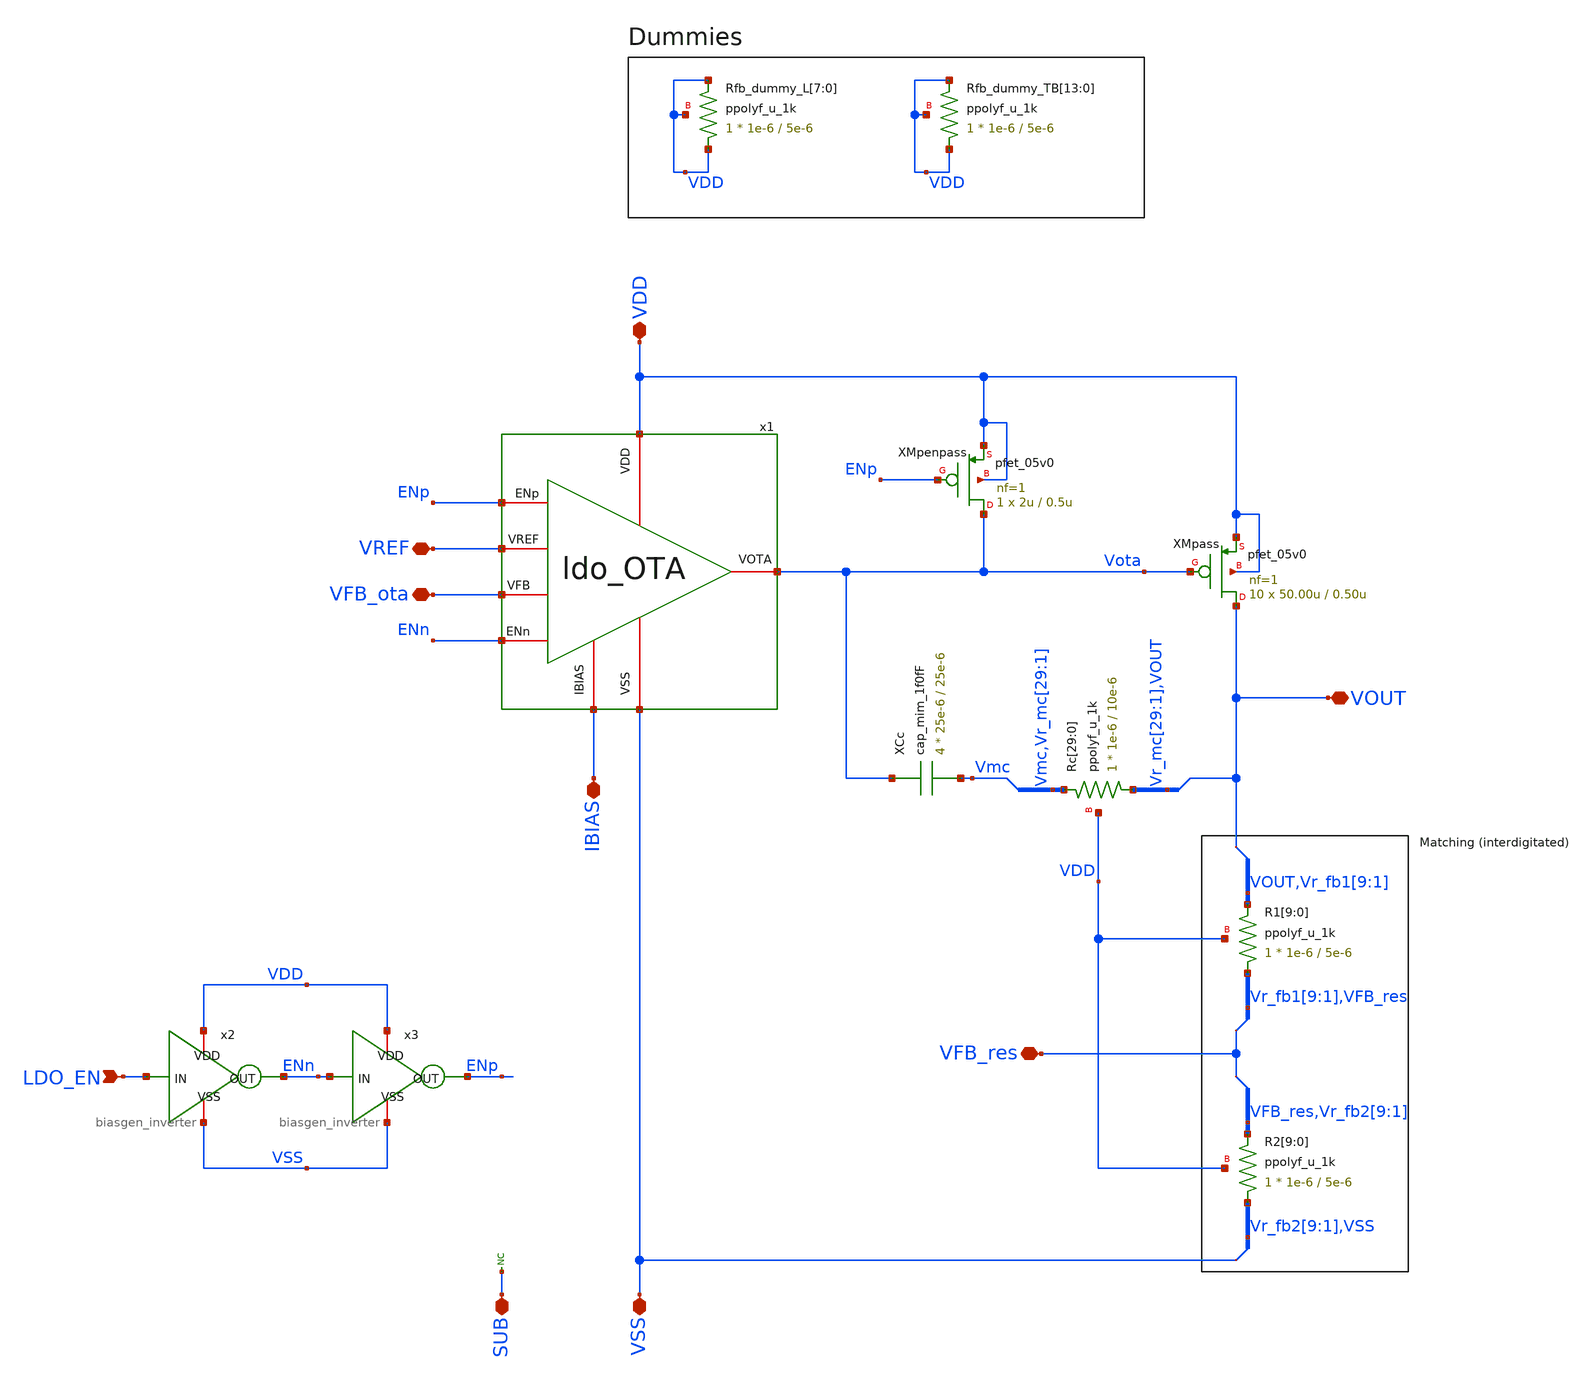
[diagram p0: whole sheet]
** sch_path: designs/libs/core_ldo/ldo/ldo.sch
**.subckt ldo VDD VSS VOUT VREF IBIAS LDO_EN VFB_ota VFB_res SUB
*.iopin VDD
*.iopin VSS
*.iopin VOUT
*.iopin VREF
*.iopin IBIAS
*.ipin LDO_EN
*.iopin VFB_ota
*.iopin VFB_res
*.iopin SUB
XMpass VOUT Vota VDD VDD pfet_05v0 L=0.50u W=50.00u nf=1 ad='int((nf+1)/2) * W/nf * 0.18u' as='int((nf+2)/2) * W/nf * 0.18u'
+ pd='2*int((nf+1)/2) * (W/nf + 0.18u)' ps='2*int((nf+2)/2) * (W/nf + 0.18u)' nrd='0.18u / W' nrs='0.18u / W'
+ sa=0 sb=0 sd=0 m=10
XR1[9] Vr_fb1[9] VOUT VDD ppolyf_u_1k r_width=1e-6 r_length=5e-6 m=1
XR1[8] Vr_fb1[8] Vr_fb1[9] VDD ppolyf_u_1k r_width=1e-6 r_length=5e-6 m=1
XR1[7] Vr_fb1[7] Vr_fb1[8] VDD ppolyf_u_1k r_width=1e-6 r_length=5e-6 m=1
XR1[6] Vr_fb1[6] Vr_fb1[7] VDD ppolyf_u_1k r_width=1e-6 r_length=5e-6 m=1
XR1[5] Vr_fb1[5] Vr_fb1[6] VDD ppolyf_u_1k r_width=1e-6 r_length=5e-6 m=1
XR1[4] Vr_fb1[4] Vr_fb1[5] VDD ppolyf_u_1k r_width=1e-6 r_length=5e-6 m=1
XR1[3] Vr_fb1[3] Vr_fb1[4] VDD ppolyf_u_1k r_width=1e-6 r_length=5e-6 m=1
XR1[2] Vr_fb1[2] Vr_fb1[3] VDD ppolyf_u_1k r_width=1e-6 r_length=5e-6 m=1
XR1[1] Vr_fb1[1] Vr_fb1[2] VDD ppolyf_u_1k r_width=1e-6 r_length=5e-6 m=1
XR1[0] VFB_res Vr_fb1[1] VDD ppolyf_u_1k r_width=1e-6 r_length=5e-6 m=1
XR2[9] Vr_fb2[9] VFB_res VDD ppolyf_u_1k r_width=1e-6 r_length=5e-6 m=1
XR2[8] Vr_fb2[8] Vr_fb2[9] VDD ppolyf_u_1k r_width=1e-6 r_length=5e-6 m=1
XR2[7] Vr_fb2[7] Vr_fb2[8] VDD ppolyf_u_1k r_width=1e-6 r_length=5e-6 m=1
XR2[6] Vr_fb2[6] Vr_fb2[7] VDD ppolyf_u_1k r_width=1e-6 r_length=5e-6 m=1
XR2[5] Vr_fb2[5] Vr_fb2[6] VDD ppolyf_u_1k r_width=1e-6 r_length=5e-6 m=1
XR2[4] Vr_fb2[4] Vr_fb2[5] VDD ppolyf_u_1k r_width=1e-6 r_length=5e-6 m=1
XR2[3] Vr_fb2[3] Vr_fb2[4] VDD ppolyf_u_1k r_width=1e-6 r_length=5e-6 m=1
XR2[2] Vr_fb2[2] Vr_fb2[3] VDD ppolyf_u_1k r_width=1e-6 r_length=5e-6 m=1
XR2[1] Vr_fb2[1] Vr_fb2[2] VDD ppolyf_u_1k r_width=1e-6 r_length=5e-6 m=1
XR2[0] VSS Vr_fb2[1] VDD ppolyf_u_1k r_width=1e-6 r_length=5e-6 m=1
XRc[29] Vr_mc[29] Vmc VDD ppolyf_u_1k r_width=1e-6 r_length=10e-6 m=1
XRc[28] Vr_mc[28] Vr_mc[29] VDD ppolyf_u_1k r_width=1e-6 r_length=10e-6 m=1
XRc[27] Vr_mc[27] Vr_mc[28] VDD ppolyf_u_1k r_width=1e-6 r_length=10e-6 m=1
XRc[26] Vr_mc[26] Vr_mc[27] VDD ppolyf_u_1k r_width=1e-6 r_length=10e-6 m=1
XRc[25] Vr_mc[25] Vr_mc[26] VDD ppolyf_u_1k r_width=1e-6 r_length=10e-6 m=1
XRc[24] Vr_mc[24] Vr_mc[25] VDD ppolyf_u_1k r_width=1e-6 r_length=10e-6 m=1
XRc[23] Vr_mc[23] Vr_mc[24] VDD ppolyf_u_1k r_width=1e-6 r_length=10e-6 m=1
XRc[22] Vr_mc[22] Vr_mc[23] VDD ppolyf_u_1k r_width=1e-6 r_length=10e-6 m=1
XRc[21] Vr_mc[21] Vr_mc[22] VDD ppolyf_u_1k r_width=1e-6 r_length=10e-6 m=1
XRc[20] Vr_mc[20] Vr_mc[21] VDD ppolyf_u_1k r_width=1e-6 r_length=10e-6 m=1
XRc[19] Vr_mc[19] Vr_mc[20] VDD ppolyf_u_1k r_width=1e-6 r_length=10e-6 m=1
XRc[18] Vr_mc[18] Vr_mc[19] VDD ppolyf_u_1k r_width=1e-6 r_length=10e-6 m=1
XRc[17] Vr_mc[17] Vr_mc[18] VDD ppolyf_u_1k r_width=1e-6 r_length=10e-6 m=1
XRc[16] Vr_mc[16] Vr_mc[17] VDD ppolyf_u_1k r_width=1e-6 r_length=10e-6 m=1
XRc[15] Vr_mc[15] Vr_mc[16] VDD ppolyf_u_1k r_width=1e-6 r_length=10e-6 m=1
XRc[14] Vr_mc[14] Vr_mc[15] VDD ppolyf_u_1k r_width=1e-6 r_length=10e-6 m=1
XRc[13] Vr_mc[13] Vr_mc[14] VDD ppolyf_u_1k r_width=1e-6 r_length=10e-6 m=1
XRc[12] Vr_mc[12] Vr_mc[13] VDD ppolyf_u_1k r_width=1e-6 r_length=10e-6 m=1
XRc[11] Vr_mc[11] Vr_mc[12] VDD ppolyf_u_1k r_width=1e-6 r_length=10e-6 m=1
XRc[10] Vr_mc[10] Vr_mc[11] VDD ppolyf_u_1k r_width=1e-6 r_length=10e-6 m=1
XRc[9] Vr_mc[9] Vr_mc[10] VDD ppolyf_u_1k r_width=1e-6 r_length=10e-6 m=1
XRc[8] Vr_mc[8] Vr_mc[9] VDD ppolyf_u_1k r_width=1e-6 r_length=10e-6 m=1
XRc[7] Vr_mc[7] Vr_mc[8] VDD ppolyf_u_1k r_width=1e-6 r_length=10e-6 m=1
XRc[6] Vr_mc[6] Vr_mc[7] VDD ppolyf_u_1k r_width=1e-6 r_length=10e-6 m=1
XRc[5] Vr_mc[5] Vr_mc[6] VDD ppolyf_u_1k r_width=1e-6 r_length=10e-6 m=1
XRc[4] Vr_mc[4] Vr_mc[5] VDD ppolyf_u_1k r_width=1e-6 r_length=10e-6 m=1
XRc[3] Vr_mc[3] Vr_mc[4] VDD ppolyf_u_1k r_width=1e-6 r_length=10e-6 m=1
XRc[2] Vr_mc[2] Vr_mc[3] VDD ppolyf_u_1k r_width=1e-6 r_length=10e-6 m=1
XRc[1] Vr_mc[1] Vr_mc[2] VDD ppolyf_u_1k r_width=1e-6 r_length=10e-6 m=1
XRc[0] VOUT Vr_mc[1] VDD ppolyf_u_1k r_width=1e-6 r_length=10e-6 m=1
XCc Vota Vmc cap_mim_1f0fF c_width=25e-6 c_length=25e-6 m=4
XRfb_dummy_L[7] VDD VDD VDD ppolyf_u_1k r_width=1e-6 r_length=5e-6 m=1
XRfb_dummy_L[6] VDD VDD VDD ppolyf_u_1k r_width=1e-6 r_length=5e-6 m=1
XRfb_dummy_L[5] VDD VDD VDD ppolyf_u_1k r_width=1e-6 r_length=5e-6 m=1
XRfb_dummy_L[4] VDD VDD VDD ppolyf_u_1k r_width=1e-6 r_length=5e-6 m=1
XRfb_dummy_L[3] VDD VDD VDD ppolyf_u_1k r_width=1e-6 r_length=5e-6 m=1
XRfb_dummy_L[2] VDD VDD VDD ppolyf_u_1k r_width=1e-6 r_length=5e-6 m=1
XRfb_dummy_L[1] VDD VDD VDD ppolyf_u_1k r_width=1e-6 r_length=5e-6 m=1
XRfb_dummy_L[0] VDD VDD VDD ppolyf_u_1k r_width=1e-6 r_length=5e-6 m=1
XRfb_dummy_TB[13] VDD VDD VDD ppolyf_u_1k r_width=1e-6 r_length=5e-6 m=1
XRfb_dummy_TB[12] VDD VDD VDD ppolyf_u_1k r_width=1e-6 r_length=5e-6 m=1
XRfb_dummy_TB[11] VDD VDD VDD ppolyf_u_1k r_width=1e-6 r_length=5e-6 m=1
XRfb_dummy_TB[10] VDD VDD VDD ppolyf_u_1k r_width=1e-6 r_length=5e-6 m=1
XRfb_dummy_TB[9] VDD VDD VDD ppolyf_u_1k r_width=1e-6 r_length=5e-6 m=1
XRfb_dummy_TB[8] VDD VDD VDD ppolyf_u_1k r_width=1e-6 r_length=5e-6 m=1
XRfb_dummy_TB[7] VDD VDD VDD ppolyf_u_1k r_width=1e-6 r_length=5e-6 m=1
XRfb_dummy_TB[6] VDD VDD VDD ppolyf_u_1k r_width=1e-6 r_length=5e-6 m=1
XRfb_dummy_TB[5] VDD VDD VDD ppolyf_u_1k r_width=1e-6 r_length=5e-6 m=1
XRfb_dummy_TB[4] VDD VDD VDD ppolyf_u_1k r_width=1e-6 r_length=5e-6 m=1
XRfb_dummy_TB[3] VDD VDD VDD ppolyf_u_1k r_width=1e-6 r_length=5e-6 m=1
XRfb_dummy_TB[2] VDD VDD VDD ppolyf_u_1k r_width=1e-6 r_length=5e-6 m=1
XRfb_dummy_TB[1] VDD VDD VDD ppolyf_u_1k r_width=1e-6 r_length=5e-6 m=1
XRfb_dummy_TB[0] VDD VDD VDD ppolyf_u_1k r_width=1e-6 r_length=5e-6 m=1
* noconn SUB
x2 VDD LDO_EN ENn VSS biasgen_inverter
x3 VDD ENn ENp VSS biasgen_inverter
XMpenpass Vota ENp VDD VDD pfet_05v0 L=0.5u W=2u nf=1 ad='int((nf+1)/2) * W/nf * 0.18u' as='int((nf+2)/2) * W/nf * 0.18u'
+ pd='2*int((nf+1)/2) * (W/nf + 0.18u)' ps='2*int((nf+2)/2) * (W/nf + 0.18u)' nrd='0.18u / W' nrs='0.18u / W'
+ sa=0 sb=0 sd=0 m=1
x1 VDD VREF VFB_ota Vota IBIAS VSS ENp ENn ldo_OTA
**.ends

* expanding   symbol:  libs/core_biasgen/biasgen_inverter/biasgen_inverter.sym # of pins=4
** sym_path: designs/libs/core_biasgen/biasgen_inverter/biasgen_inverter.sym
** sch_path: designs/libs/core_biasgen/biasgen_inverter/biasgen_inverter.sch
.subckt biasgen_inverter VDD IN OUT VSS
*.iopin VDD
*.iopin VSS
*.ipin IN
*.opin OUT
XMINV1 OUT IN VSS VSS nfet_05v0 L=0.60u W=0.50u nf=1 ad='int((nf+1)/2) * W/nf * 0.18u' as='int((nf+2)/2) * W/nf * 0.18u'
+ pd='2*int((nf+1)/2) * (W/nf + 0.18u)' ps='2*int((nf+2)/2) * (W/nf + 0.18u)' nrd='0.18u / W' nrs='0.18u / W'
+ sa=0 sb=0 sd=0 m=1
XMINV2 OUT IN VDD VDD pfet_05v0 L=0.50u W=0.60u nf=1 ad='int((nf+1)/2) * W/nf * 0.18u' as='int((nf+2)/2) * W/nf * 0.18u'
+ pd='2*int((nf+1)/2) * (W/nf + 0.18u)' ps='2*int((nf+2)/2) * (W/nf + 0.18u)' nrd='0.18u / W' nrs='0.18u / W'
+ sa=0 sb=0 sd=0 m=1
.ends


* expanding   symbol:  libs/core_ldo/ldo_OTA/ldo_OTA.sym # of pins=8
** sym_path: designs/libs/core_ldo/ldo_OTA/ldo_OTA.sym
** sch_path: designs/libs/core_ldo/ldo_OTA/ldo_OTA.sch
.subckt ldo_OTA VDD VREF VFB VOTA IBIAS VSS ENp ENn
*.iopin VDD
*.iopin VSS
*.iopin VOTA
*.iopin VREF
*.iopin IBIAS
*.iopin VFB
*.ipin ENp
*.ipin ENn
XM3 Vbp1 Vbp1 VDD VDD pfet_05v0 L=1.00u W=5.50u nf=1 ad='int((nf+1)/2) * W/nf * 0.18u' as='int((nf+2)/2) * W/nf * 0.18u'
+ pd='2*int((nf+1)/2) * (W/nf + 0.18u)' ps='2*int((nf+2)/2) * (W/nf + 0.18u)' nrd='0.18u / W' nrs='0.18u / W'
+ sa=0 sb=0 sd=0 m=2
XM4 Vbp2 Vbp2 VDD VDD pfet_05v0 L=1.00u W=5.50u nf=1 ad='int((nf+1)/2) * W/nf * 0.18u' as='int((nf+2)/2) * W/nf * 0.18u'
+ pd='2*int((nf+1)/2) * (W/nf + 0.18u)' ps='2*int((nf+2)/2) * (W/nf + 0.18u)' nrd='0.18u / W' nrs='0.18u / W'
+ sa=0 sb=0 sd=0 m=2
XM5 Vbn2 Vbp1 VDD VDD pfet_05v0 L=1.00u W=5.50u nf=1 ad='int((nf+1)/2) * W/nf * 0.18u' as='int((nf+2)/2) * W/nf * 0.18u'
+ pd='2*int((nf+1)/2) * (W/nf + 0.18u)' ps='2*int((nf+2)/2) * (W/nf + 0.18u)' nrd='0.18u / W' nrs='0.18u / W'
+ sa=0 sb=0 sd=0 m=2
XM6 VOTA Vbp2 VDD VDD pfet_05v0 L=1.00u W=5.50u nf=1 ad='int((nf+1)/2) * W/nf * 0.18u' as='int((nf+2)/2) * W/nf * 0.18u'
+ pd='2*int((nf+1)/2) * (W/nf + 0.18u)' ps='2*int((nf+2)/2) * (W/nf + 0.18u)' nrd='0.18u / W' nrs='0.18u / W'
+ sa=0 sb=0 sd=0 m=6
XM9 Vbn1 Vbn1 VSS VSS nfet_05v0 L=1.00u W=3.00u nf=1 ad='int((nf+1)/2) * W/nf * 0.18u' as='int((nf+2)/2) * W/nf * 0.18u'
+ pd='2*int((nf+1)/2) * (W/nf + 0.18u)' ps='2*int((nf+2)/2) * (W/nf + 0.18u)' nrd='0.18u / W' nrs='0.18u / W'
+ sa=0 sb=0 sd=0 m=2
XM10 Vtail Vbn1 VSS VSS nfet_05v0 L=1.00u W=3.00u nf=1 ad='int((nf+1)/2) * W/nf * 0.18u' as='int((nf+2)/2) * W/nf * 0.18u'
+ pd='2*int((nf+1)/2) * (W/nf + 0.18u)' ps='2*int((nf+2)/2) * (W/nf + 0.18u)' nrd='0.18u / W' nrs='0.18u / W'
+ sa=0 sb=0 sd=0 m=2
XM7 Vbn2 Vbn2 VSS VSS nfet_05v0 L=1.00u W=1.25u nf=1 ad='int((nf+1)/2) * W/nf * 0.18u' as='int((nf+2)/2) * W/nf * 0.18u'
+ pd='2*int((nf+1)/2) * (W/nf + 0.18u)' ps='2*int((nf+2)/2) * (W/nf + 0.18u)' nrd='0.18u / W' nrs='0.18u / W'
+ sa=0 sb=0 sd=0 m=2
XM8 VOTA Vbn2 VSS VSS nfet_05v0 L=1.00u W=1.25u nf=1 ad='int((nf+1)/2) * W/nf * 0.18u' as='int((nf+2)/2) * W/nf * 0.18u'
+ pd='2*int((nf+1)/2) * (W/nf + 0.18u)' ps='2*int((nf+2)/2) * (W/nf + 0.18u)' nrd='0.18u / W' nrs='0.18u / W'
+ sa=0 sb=0 sd=0 m=6
XM1 Vbp1 VREF Vtail VSS nfet_05v0 L=0.60u W=5.00u nf=1 ad='int((nf+1)/2) * W/nf * 0.18u' as='int((nf+2)/2) * W/nf * 0.18u'
+ pd='2*int((nf+1)/2) * (W/nf + 0.18u)' ps='2*int((nf+2)/2) * (W/nf + 0.18u)' nrd='0.18u / W' nrs='0.18u / W'
+ sa=0 sb=0 sd=0 m=14
XM2 Vbp2 VFB Vtail VSS nfet_05v0 L=0.60u W=5.00u nf=1 ad='int((nf+1)/2) * W/nf * 0.18u' as='int((nf+2)/2) * W/nf * 0.18u'
+ pd='2*int((nf+1)/2) * (W/nf + 0.18u)' ps='2*int((nf+2)/2) * (W/nf + 0.18u)' nrd='0.18u / W' nrs='0.18u / W'
+ sa=0 sb=0 sd=0 m=14
XMpota_dummy_L[3] VDD VDD VDD VDD pfet_05v0 L=1.00u W=5.50u nf=1 ad='int((nf+1)/2) * W/nf * 0.18u' as='int((nf+2)/2) * W/nf * 0.18u'
+ pd='2*int((nf+1)/2) * (W/nf + 0.18u)' ps='2*int((nf+2)/2) * (W/nf + 0.18u)' nrd='0.18u / W' nrs='0.18u / W'
+ sa=0 sb=0 sd=0 m=1
XMpota_dummy_L[2] VDD VDD VDD VDD pfet_05v0 L=1.00u W=5.50u nf=1 ad='int((nf+1)/2) * W/nf * 0.18u' as='int((nf+2)/2) * W/nf * 0.18u'
+ pd='2*int((nf+1)/2) * (W/nf + 0.18u)' ps='2*int((nf+2)/2) * (W/nf + 0.18u)' nrd='0.18u / W' nrs='0.18u / W'
+ sa=0 sb=0 sd=0 m=1
XMpota_dummy_L[1] VDD VDD VDD VDD pfet_05v0 L=1.00u W=5.50u nf=1 ad='int((nf+1)/2) * W/nf * 0.18u' as='int((nf+2)/2) * W/nf * 0.18u'
+ pd='2*int((nf+1)/2) * (W/nf + 0.18u)' ps='2*int((nf+2)/2) * (W/nf + 0.18u)' nrd='0.18u / W' nrs='0.18u / W'
+ sa=0 sb=0 sd=0 m=1
XMpota_dummy_L[0] VDD VDD VDD VDD pfet_05v0 L=1.00u W=5.50u nf=1 ad='int((nf+1)/2) * W/nf * 0.18u' as='int((nf+2)/2) * W/nf * 0.18u'
+ pd='2*int((nf+1)/2) * (W/nf + 0.18u)' ps='2*int((nf+2)/2) * (W/nf + 0.18u)' nrd='0.18u / W' nrs='0.18u / W'
+ sa=0 sb=0 sd=0 m=1
XMpota_dummy_TB[15] VDD VDD VDD VDD pfet_05v0 L=1.00u W=5.50u nf=1 ad='int((nf+1)/2) * W/nf * 0.18u'
+ as='int((nf+2)/2) * W/nf * 0.18u' pd='2*int((nf+1)/2) * (W/nf + 0.18u)' ps='2*int((nf+2)/2) * (W/nf + 0.18u)'
+ nrd='0.18u / W' nrs='0.18u / W' sa=0 sb=0 sd=0 m=1
XMpota_dummy_TB[14] VDD VDD VDD VDD pfet_05v0 L=1.00u W=5.50u nf=1 ad='int((nf+1)/2) * W/nf * 0.18u'
+ as='int((nf+2)/2) * W/nf * 0.18u' pd='2*int((nf+1)/2) * (W/nf + 0.18u)' ps='2*int((nf+2)/2) * (W/nf + 0.18u)'
+ nrd='0.18u / W' nrs='0.18u / W' sa=0 sb=0 sd=0 m=1
XMpota_dummy_TB[13] VDD VDD VDD VDD pfet_05v0 L=1.00u W=5.50u nf=1 ad='int((nf+1)/2) * W/nf * 0.18u'
+ as='int((nf+2)/2) * W/nf * 0.18u' pd='2*int((nf+1)/2) * (W/nf + 0.18u)' ps='2*int((nf+2)/2) * (W/nf + 0.18u)'
+ nrd='0.18u / W' nrs='0.18u / W' sa=0 sb=0 sd=0 m=1
XMpota_dummy_TB[12] VDD VDD VDD VDD pfet_05v0 L=1.00u W=5.50u nf=1 ad='int((nf+1)/2) * W/nf * 0.18u'
+ as='int((nf+2)/2) * W/nf * 0.18u' pd='2*int((nf+1)/2) * (W/nf + 0.18u)' ps='2*int((nf+2)/2) * (W/nf + 0.18u)'
+ nrd='0.18u / W' nrs='0.18u / W' sa=0 sb=0 sd=0 m=1
XMpota_dummy_TB[11] VDD VDD VDD VDD pfet_05v0 L=1.00u W=5.50u nf=1 ad='int((nf+1)/2) * W/nf * 0.18u'
+ as='int((nf+2)/2) * W/nf * 0.18u' pd='2*int((nf+1)/2) * (W/nf + 0.18u)' ps='2*int((nf+2)/2) * (W/nf + 0.18u)'
+ nrd='0.18u / W' nrs='0.18u / W' sa=0 sb=0 sd=0 m=1
XMpota_dummy_TB[10] VDD VDD VDD VDD pfet_05v0 L=1.00u W=5.50u nf=1 ad='int((nf+1)/2) * W/nf * 0.18u'
+ as='int((nf+2)/2) * W/nf * 0.18u' pd='2*int((nf+1)/2) * (W/nf + 0.18u)' ps='2*int((nf+2)/2) * (W/nf + 0.18u)'
+ nrd='0.18u / W' nrs='0.18u / W' sa=0 sb=0 sd=0 m=1
XMpota_dummy_TB[9] VDD VDD VDD VDD pfet_05v0 L=1.00u W=5.50u nf=1 ad='int((nf+1)/2) * W/nf * 0.18u' as='int((nf+2)/2) * W/nf * 0.18u'
+ pd='2*int((nf+1)/2) * (W/nf + 0.18u)' ps='2*int((nf+2)/2) * (W/nf + 0.18u)' nrd='0.18u / W' nrs='0.18u / W'
+ sa=0 sb=0 sd=0 m=1
XMpota_dummy_TB[8] VDD VDD VDD VDD pfet_05v0 L=1.00u W=5.50u nf=1 ad='int((nf+1)/2) * W/nf * 0.18u' as='int((nf+2)/2) * W/nf * 0.18u'
+ pd='2*int((nf+1)/2) * (W/nf + 0.18u)' ps='2*int((nf+2)/2) * (W/nf + 0.18u)' nrd='0.18u / W' nrs='0.18u / W'
+ sa=0 sb=0 sd=0 m=1
XMpota_dummy_TB[7] VDD VDD VDD VDD pfet_05v0 L=1.00u W=5.50u nf=1 ad='int((nf+1)/2) * W/nf * 0.18u' as='int((nf+2)/2) * W/nf * 0.18u'
+ pd='2*int((nf+1)/2) * (W/nf + 0.18u)' ps='2*int((nf+2)/2) * (W/nf + 0.18u)' nrd='0.18u / W' nrs='0.18u / W'
+ sa=0 sb=0 sd=0 m=1
XMpota_dummy_TB[6] VDD VDD VDD VDD pfet_05v0 L=1.00u W=5.50u nf=1 ad='int((nf+1)/2) * W/nf * 0.18u' as='int((nf+2)/2) * W/nf * 0.18u'
+ pd='2*int((nf+1)/2) * (W/nf + 0.18u)' ps='2*int((nf+2)/2) * (W/nf + 0.18u)' nrd='0.18u / W' nrs='0.18u / W'
+ sa=0 sb=0 sd=0 m=1
XMpota_dummy_TB[5] VDD VDD VDD VDD pfet_05v0 L=1.00u W=5.50u nf=1 ad='int((nf+1)/2) * W/nf * 0.18u' as='int((nf+2)/2) * W/nf * 0.18u'
+ pd='2*int((nf+1)/2) * (W/nf + 0.18u)' ps='2*int((nf+2)/2) * (W/nf + 0.18u)' nrd='0.18u / W' nrs='0.18u / W'
+ sa=0 sb=0 sd=0 m=1
XMpota_dummy_TB[4] VDD VDD VDD VDD pfet_05v0 L=1.00u W=5.50u nf=1 ad='int((nf+1)/2) * W/nf * 0.18u' as='int((nf+2)/2) * W/nf * 0.18u'
+ pd='2*int((nf+1)/2) * (W/nf + 0.18u)' ps='2*int((nf+2)/2) * (W/nf + 0.18u)' nrd='0.18u / W' nrs='0.18u / W'
+ sa=0 sb=0 sd=0 m=1
XMpota_dummy_TB[3] VDD VDD VDD VDD pfet_05v0 L=1.00u W=5.50u nf=1 ad='int((nf+1)/2) * W/nf * 0.18u' as='int((nf+2)/2) * W/nf * 0.18u'
+ pd='2*int((nf+1)/2) * (W/nf + 0.18u)' ps='2*int((nf+2)/2) * (W/nf + 0.18u)' nrd='0.18u / W' nrs='0.18u / W'
+ sa=0 sb=0 sd=0 m=1
XMpota_dummy_TB[2] VDD VDD VDD VDD pfet_05v0 L=1.00u W=5.50u nf=1 ad='int((nf+1)/2) * W/nf * 0.18u' as='int((nf+2)/2) * W/nf * 0.18u'
+ pd='2*int((nf+1)/2) * (W/nf + 0.18u)' ps='2*int((nf+2)/2) * (W/nf + 0.18u)' nrd='0.18u / W' nrs='0.18u / W'
+ sa=0 sb=0 sd=0 m=1
XMpota_dummy_TB[1] VDD VDD VDD VDD pfet_05v0 L=1.00u W=5.50u nf=1 ad='int((nf+1)/2) * W/nf * 0.18u' as='int((nf+2)/2) * W/nf * 0.18u'
+ pd='2*int((nf+1)/2) * (W/nf + 0.18u)' ps='2*int((nf+2)/2) * (W/nf + 0.18u)' nrd='0.18u / W' nrs='0.18u / W'
+ sa=0 sb=0 sd=0 m=1
XMpota_dummy_TB[0] VDD VDD VDD VDD pfet_05v0 L=1.00u W=5.50u nf=1 ad='int((nf+1)/2) * W/nf * 0.18u' as='int((nf+2)/2) * W/nf * 0.18u'
+ pd='2*int((nf+1)/2) * (W/nf + 0.18u)' ps='2*int((nf+2)/2) * (W/nf + 0.18u)' nrd='0.18u / W' nrs='0.18u / W'
+ sa=0 sb=0 sd=0 m=1
XMndiff_dummy_L[7] VSS VSS VSS VSS nfet_05v0 L=0.60u W=5.00u nf=1 ad='int((nf+1)/2) * W/nf * 0.18u' as='int((nf+2)/2) * W/nf * 0.18u'
+ pd='2*int((nf+1)/2) * (W/nf + 0.18u)' ps='2*int((nf+2)/2) * (W/nf + 0.18u)' nrd='0.18u / W' nrs='0.18u / W'
+ sa=0 sb=0 sd=0 m=1
XMndiff_dummy_L[6] VSS VSS VSS VSS nfet_05v0 L=0.60u W=5.00u nf=1 ad='int((nf+1)/2) * W/nf * 0.18u' as='int((nf+2)/2) * W/nf * 0.18u'
+ pd='2*int((nf+1)/2) * (W/nf + 0.18u)' ps='2*int((nf+2)/2) * (W/nf + 0.18u)' nrd='0.18u / W' nrs='0.18u / W'
+ sa=0 sb=0 sd=0 m=1
XMndiff_dummy_L[5] VSS VSS VSS VSS nfet_05v0 L=0.60u W=5.00u nf=1 ad='int((nf+1)/2) * W/nf * 0.18u' as='int((nf+2)/2) * W/nf * 0.18u'
+ pd='2*int((nf+1)/2) * (W/nf + 0.18u)' ps='2*int((nf+2)/2) * (W/nf + 0.18u)' nrd='0.18u / W' nrs='0.18u / W'
+ sa=0 sb=0 sd=0 m=1
XMndiff_dummy_L[4] VSS VSS VSS VSS nfet_05v0 L=0.60u W=5.00u nf=1 ad='int((nf+1)/2) * W/nf * 0.18u' as='int((nf+2)/2) * W/nf * 0.18u'
+ pd='2*int((nf+1)/2) * (W/nf + 0.18u)' ps='2*int((nf+2)/2) * (W/nf + 0.18u)' nrd='0.18u / W' nrs='0.18u / W'
+ sa=0 sb=0 sd=0 m=1
XMndiff_dummy_L[3] VSS VSS VSS VSS nfet_05v0 L=0.60u W=5.00u nf=1 ad='int((nf+1)/2) * W/nf * 0.18u' as='int((nf+2)/2) * W/nf * 0.18u'
+ pd='2*int((nf+1)/2) * (W/nf + 0.18u)' ps='2*int((nf+2)/2) * (W/nf + 0.18u)' nrd='0.18u / W' nrs='0.18u / W'
+ sa=0 sb=0 sd=0 m=1
XMndiff_dummy_L[2] VSS VSS VSS VSS nfet_05v0 L=0.60u W=5.00u nf=1 ad='int((nf+1)/2) * W/nf * 0.18u' as='int((nf+2)/2) * W/nf * 0.18u'
+ pd='2*int((nf+1)/2) * (W/nf + 0.18u)' ps='2*int((nf+2)/2) * (W/nf + 0.18u)' nrd='0.18u / W' nrs='0.18u / W'
+ sa=0 sb=0 sd=0 m=1
XMndiff_dummy_L[1] VSS VSS VSS VSS nfet_05v0 L=0.60u W=5.00u nf=1 ad='int((nf+1)/2) * W/nf * 0.18u' as='int((nf+2)/2) * W/nf * 0.18u'
+ pd='2*int((nf+1)/2) * (W/nf + 0.18u)' ps='2*int((nf+2)/2) * (W/nf + 0.18u)' nrd='0.18u / W' nrs='0.18u / W'
+ sa=0 sb=0 sd=0 m=1
XMndiff_dummy_L[0] VSS VSS VSS VSS nfet_05v0 L=0.60u W=5.00u nf=1 ad='int((nf+1)/2) * W/nf * 0.18u' as='int((nf+2)/2) * W/nf * 0.18u'
+ pd='2*int((nf+1)/2) * (W/nf + 0.18u)' ps='2*int((nf+2)/2) * (W/nf + 0.18u)' nrd='0.18u / W' nrs='0.18u / W'
+ sa=0 sb=0 sd=0 m=1
XMndiff_dummy_TB[17] VSS VSS VSS VSS nfet_05v0 L=0.60u W=5.00u nf=1 ad='int((nf+1)/2) * W/nf * 0.18u'
+ as='int((nf+2)/2) * W/nf * 0.18u' pd='2*int((nf+1)/2) * (W/nf + 0.18u)' ps='2*int((nf+2)/2) * (W/nf + 0.18u)'
+ nrd='0.18u / W' nrs='0.18u / W' sa=0 sb=0 sd=0 m=1
XMndiff_dummy_TB[16] VSS VSS VSS VSS nfet_05v0 L=0.60u W=5.00u nf=1 ad='int((nf+1)/2) * W/nf * 0.18u'
+ as='int((nf+2)/2) * W/nf * 0.18u' pd='2*int((nf+1)/2) * (W/nf + 0.18u)' ps='2*int((nf+2)/2) * (W/nf + 0.18u)'
+ nrd='0.18u / W' nrs='0.18u / W' sa=0 sb=0 sd=0 m=1
XMndiff_dummy_TB[15] VSS VSS VSS VSS nfet_05v0 L=0.60u W=5.00u nf=1 ad='int((nf+1)/2) * W/nf * 0.18u'
+ as='int((nf+2)/2) * W/nf * 0.18u' pd='2*int((nf+1)/2) * (W/nf + 0.18u)' ps='2*int((nf+2)/2) * (W/nf + 0.18u)'
+ nrd='0.18u / W' nrs='0.18u / W' sa=0 sb=0 sd=0 m=1
XMndiff_dummy_TB[14] VSS VSS VSS VSS nfet_05v0 L=0.60u W=5.00u nf=1 ad='int((nf+1)/2) * W/nf * 0.18u'
+ as='int((nf+2)/2) * W/nf * 0.18u' pd='2*int((nf+1)/2) * (W/nf + 0.18u)' ps='2*int((nf+2)/2) * (W/nf + 0.18u)'
+ nrd='0.18u / W' nrs='0.18u / W' sa=0 sb=0 sd=0 m=1
XMndiff_dummy_TB[13] VSS VSS VSS VSS nfet_05v0 L=0.60u W=5.00u nf=1 ad='int((nf+1)/2) * W/nf * 0.18u'
+ as='int((nf+2)/2) * W/nf * 0.18u' pd='2*int((nf+1)/2) * (W/nf + 0.18u)' ps='2*int((nf+2)/2) * (W/nf + 0.18u)'
+ nrd='0.18u / W' nrs='0.18u / W' sa=0 sb=0 sd=0 m=1
XMndiff_dummy_TB[12] VSS VSS VSS VSS nfet_05v0 L=0.60u W=5.00u nf=1 ad='int((nf+1)/2) * W/nf * 0.18u'
+ as='int((nf+2)/2) * W/nf * 0.18u' pd='2*int((nf+1)/2) * (W/nf + 0.18u)' ps='2*int((nf+2)/2) * (W/nf + 0.18u)'
+ nrd='0.18u / W' nrs='0.18u / W' sa=0 sb=0 sd=0 m=1
XMndiff_dummy_TB[11] VSS VSS VSS VSS nfet_05v0 L=0.60u W=5.00u nf=1 ad='int((nf+1)/2) * W/nf * 0.18u'
+ as='int((nf+2)/2) * W/nf * 0.18u' pd='2*int((nf+1)/2) * (W/nf + 0.18u)' ps='2*int((nf+2)/2) * (W/nf + 0.18u)'
+ nrd='0.18u / W' nrs='0.18u / W' sa=0 sb=0 sd=0 m=1
XMndiff_dummy_TB[10] VSS VSS VSS VSS nfet_05v0 L=0.60u W=5.00u nf=1 ad='int((nf+1)/2) * W/nf * 0.18u'
+ as='int((nf+2)/2) * W/nf * 0.18u' pd='2*int((nf+1)/2) * (W/nf + 0.18u)' ps='2*int((nf+2)/2) * (W/nf + 0.18u)'
+ nrd='0.18u / W' nrs='0.18u / W' sa=0 sb=0 sd=0 m=1
XMndiff_dummy_TB[9] VSS VSS VSS VSS nfet_05v0 L=0.60u W=5.00u nf=1 ad='int((nf+1)/2) * W/nf * 0.18u'
+ as='int((nf+2)/2) * W/nf * 0.18u' pd='2*int((nf+1)/2) * (W/nf + 0.18u)' ps='2*int((nf+2)/2) * (W/nf + 0.18u)'
+ nrd='0.18u / W' nrs='0.18u / W' sa=0 sb=0 sd=0 m=1
XMndiff_dummy_TB[8] VSS VSS VSS VSS nfet_05v0 L=0.60u W=5.00u nf=1 ad='int((nf+1)/2) * W/nf * 0.18u'
+ as='int((nf+2)/2) * W/nf * 0.18u' pd='2*int((nf+1)/2) * (W/nf + 0.18u)' ps='2*int((nf+2)/2) * (W/nf + 0.18u)'
+ nrd='0.18u / W' nrs='0.18u / W' sa=0 sb=0 sd=0 m=1
XMndiff_dummy_TB[7] VSS VSS VSS VSS nfet_05v0 L=0.60u W=5.00u nf=1 ad='int((nf+1)/2) * W/nf * 0.18u'
+ as='int((nf+2)/2) * W/nf * 0.18u' pd='2*int((nf+1)/2) * (W/nf + 0.18u)' ps='2*int((nf+2)/2) * (W/nf + 0.18u)'
+ nrd='0.18u / W' nrs='0.18u / W' sa=0 sb=0 sd=0 m=1
XMndiff_dummy_TB[6] VSS VSS VSS VSS nfet_05v0 L=0.60u W=5.00u nf=1 ad='int((nf+1)/2) * W/nf * 0.18u'
+ as='int((nf+2)/2) * W/nf * 0.18u' pd='2*int((nf+1)/2) * (W/nf + 0.18u)' ps='2*int((nf+2)/2) * (W/nf + 0.18u)'
+ nrd='0.18u / W' nrs='0.18u / W' sa=0 sb=0 sd=0 m=1
XMndiff_dummy_TB[5] VSS VSS VSS VSS nfet_05v0 L=0.60u W=5.00u nf=1 ad='int((nf+1)/2) * W/nf * 0.18u'
+ as='int((nf+2)/2) * W/nf * 0.18u' pd='2*int((nf+1)/2) * (W/nf + 0.18u)' ps='2*int((nf+2)/2) * (W/nf + 0.18u)'
+ nrd='0.18u / W' nrs='0.18u / W' sa=0 sb=0 sd=0 m=1
XMndiff_dummy_TB[4] VSS VSS VSS VSS nfet_05v0 L=0.60u W=5.00u nf=1 ad='int((nf+1)/2) * W/nf * 0.18u'
+ as='int((nf+2)/2) * W/nf * 0.18u' pd='2*int((nf+1)/2) * (W/nf + 0.18u)' ps='2*int((nf+2)/2) * (W/nf + 0.18u)'
+ nrd='0.18u / W' nrs='0.18u / W' sa=0 sb=0 sd=0 m=1
XMndiff_dummy_TB[3] VSS VSS VSS VSS nfet_05v0 L=0.60u W=5.00u nf=1 ad='int((nf+1)/2) * W/nf * 0.18u'
+ as='int((nf+2)/2) * W/nf * 0.18u' pd='2*int((nf+1)/2) * (W/nf + 0.18u)' ps='2*int((nf+2)/2) * (W/nf + 0.18u)'
+ nrd='0.18u / W' nrs='0.18u / W' sa=0 sb=0 sd=0 m=1
XMndiff_dummy_TB[2] VSS VSS VSS VSS nfet_05v0 L=0.60u W=5.00u nf=1 ad='int((nf+1)/2) * W/nf * 0.18u'
+ as='int((nf+2)/2) * W/nf * 0.18u' pd='2*int((nf+1)/2) * (W/nf + 0.18u)' ps='2*int((nf+2)/2) * (W/nf + 0.18u)'
+ nrd='0.18u / W' nrs='0.18u / W' sa=0 sb=0 sd=0 m=1
XMndiff_dummy_TB[1] VSS VSS VSS VSS nfet_05v0 L=0.60u W=5.00u nf=1 ad='int((nf+1)/2) * W/nf * 0.18u'
+ as='int((nf+2)/2) * W/nf * 0.18u' pd='2*int((nf+1)/2) * (W/nf + 0.18u)' ps='2*int((nf+2)/2) * (W/nf + 0.18u)'
+ nrd='0.18u / W' nrs='0.18u / W' sa=0 sb=0 sd=0 m=1
XMndiff_dummy_TB[0] VSS VSS VSS VSS nfet_05v0 L=0.60u W=5.00u nf=1 ad='int((nf+1)/2) * W/nf * 0.18u'
+ as='int((nf+2)/2) * W/nf * 0.18u' pd='2*int((nf+1)/2) * (W/nf + 0.18u)' ps='2*int((nf+2)/2) * (W/nf + 0.18u)'
+ nrd='0.18u / W' nrs='0.18u / W' sa=0 sb=0 sd=0 m=1
XMnota_dummy_L[3] VSS VSS VSS VSS nfet_05v0 L=1.00u W=1.25u nf=1 ad='int((nf+1)/2) * W/nf * 0.18u' as='int((nf+2)/2) * W/nf * 0.18u'
+ pd='2*int((nf+1)/2) * (W/nf + 0.18u)' ps='2*int((nf+2)/2) * (W/nf + 0.18u)' nrd='0.18u / W' nrs='0.18u / W'
+ sa=0 sb=0 sd=0 m=1
XMnota_dummy_L[2] VSS VSS VSS VSS nfet_05v0 L=1.00u W=1.25u nf=1 ad='int((nf+1)/2) * W/nf * 0.18u' as='int((nf+2)/2) * W/nf * 0.18u'
+ pd='2*int((nf+1)/2) * (W/nf + 0.18u)' ps='2*int((nf+2)/2) * (W/nf + 0.18u)' nrd='0.18u / W' nrs='0.18u / W'
+ sa=0 sb=0 sd=0 m=1
XMnota_dummy_L[1] VSS VSS VSS VSS nfet_05v0 L=1.00u W=1.25u nf=1 ad='int((nf+1)/2) * W/nf * 0.18u' as='int((nf+2)/2) * W/nf * 0.18u'
+ pd='2*int((nf+1)/2) * (W/nf + 0.18u)' ps='2*int((nf+2)/2) * (W/nf + 0.18u)' nrd='0.18u / W' nrs='0.18u / W'
+ sa=0 sb=0 sd=0 m=1
XMnota_dummy_L[0] VSS VSS VSS VSS nfet_05v0 L=1.00u W=1.25u nf=1 ad='int((nf+1)/2) * W/nf * 0.18u' as='int((nf+2)/2) * W/nf * 0.18u'
+ pd='2*int((nf+1)/2) * (W/nf + 0.18u)' ps='2*int((nf+2)/2) * (W/nf + 0.18u)' nrd='0.18u / W' nrs='0.18u / W'
+ sa=0 sb=0 sd=0 m=1
XMnota_dummy_TB[11] VSS VSS VSS VSS nfet_05v0 L=1.00u W=1.25u nf=1 ad='int((nf+1)/2) * W/nf * 0.18u'
+ as='int((nf+2)/2) * W/nf * 0.18u' pd='2*int((nf+1)/2) * (W/nf + 0.18u)' ps='2*int((nf+2)/2) * (W/nf + 0.18u)'
+ nrd='0.18u / W' nrs='0.18u / W' sa=0 sb=0 sd=0 m=1
XMnota_dummy_TB[10] VSS VSS VSS VSS nfet_05v0 L=1.00u W=1.25u nf=1 ad='int((nf+1)/2) * W/nf * 0.18u'
+ as='int((nf+2)/2) * W/nf * 0.18u' pd='2*int((nf+1)/2) * (W/nf + 0.18u)' ps='2*int((nf+2)/2) * (W/nf + 0.18u)'
+ nrd='0.18u / W' nrs='0.18u / W' sa=0 sb=0 sd=0 m=1
XMnota_dummy_TB[9] VSS VSS VSS VSS nfet_05v0 L=1.00u W=1.25u nf=1 ad='int((nf+1)/2) * W/nf * 0.18u' as='int((nf+2)/2) * W/nf * 0.18u'
+ pd='2*int((nf+1)/2) * (W/nf + 0.18u)' ps='2*int((nf+2)/2) * (W/nf + 0.18u)' nrd='0.18u / W' nrs='0.18u / W'
+ sa=0 sb=0 sd=0 m=1
XMnota_dummy_TB[8] VSS VSS VSS VSS nfet_05v0 L=1.00u W=1.25u nf=1 ad='int((nf+1)/2) * W/nf * 0.18u' as='int((nf+2)/2) * W/nf * 0.18u'
+ pd='2*int((nf+1)/2) * (W/nf + 0.18u)' ps='2*int((nf+2)/2) * (W/nf + 0.18u)' nrd='0.18u / W' nrs='0.18u / W'
+ sa=0 sb=0 sd=0 m=1
XMnota_dummy_TB[7] VSS VSS VSS VSS nfet_05v0 L=1.00u W=1.25u nf=1 ad='int((nf+1)/2) * W/nf * 0.18u' as='int((nf+2)/2) * W/nf * 0.18u'
+ pd='2*int((nf+1)/2) * (W/nf + 0.18u)' ps='2*int((nf+2)/2) * (W/nf + 0.18u)' nrd='0.18u / W' nrs='0.18u / W'
+ sa=0 sb=0 sd=0 m=1
XMnota_dummy_TB[6] VSS VSS VSS VSS nfet_05v0 L=1.00u W=1.25u nf=1 ad='int((nf+1)/2) * W/nf * 0.18u' as='int((nf+2)/2) * W/nf * 0.18u'
+ pd='2*int((nf+1)/2) * (W/nf + 0.18u)' ps='2*int((nf+2)/2) * (W/nf + 0.18u)' nrd='0.18u / W' nrs='0.18u / W'
+ sa=0 sb=0 sd=0 m=1
XMnota_dummy_TB[5] VSS VSS VSS VSS nfet_05v0 L=1.00u W=1.25u nf=1 ad='int((nf+1)/2) * W/nf * 0.18u' as='int((nf+2)/2) * W/nf * 0.18u'
+ pd='2*int((nf+1)/2) * (W/nf + 0.18u)' ps='2*int((nf+2)/2) * (W/nf + 0.18u)' nrd='0.18u / W' nrs='0.18u / W'
+ sa=0 sb=0 sd=0 m=1
XMnota_dummy_TB[4] VSS VSS VSS VSS nfet_05v0 L=1.00u W=1.25u nf=1 ad='int((nf+1)/2) * W/nf * 0.18u' as='int((nf+2)/2) * W/nf * 0.18u'
+ pd='2*int((nf+1)/2) * (W/nf + 0.18u)' ps='2*int((nf+2)/2) * (W/nf + 0.18u)' nrd='0.18u / W' nrs='0.18u / W'
+ sa=0 sb=0 sd=0 m=1
XMnota_dummy_TB[3] VSS VSS VSS VSS nfet_05v0 L=1.00u W=1.25u nf=1 ad='int((nf+1)/2) * W/nf * 0.18u' as='int((nf+2)/2) * W/nf * 0.18u'
+ pd='2*int((nf+1)/2) * (W/nf + 0.18u)' ps='2*int((nf+2)/2) * (W/nf + 0.18u)' nrd='0.18u / W' nrs='0.18u / W'
+ sa=0 sb=0 sd=0 m=1
XMnota_dummy_TB[2] VSS VSS VSS VSS nfet_05v0 L=1.00u W=1.25u nf=1 ad='int((nf+1)/2) * W/nf * 0.18u' as='int((nf+2)/2) * W/nf * 0.18u'
+ pd='2*int((nf+1)/2) * (W/nf + 0.18u)' ps='2*int((nf+2)/2) * (W/nf + 0.18u)' nrd='0.18u / W' nrs='0.18u / W'
+ sa=0 sb=0 sd=0 m=1
XMnota_dummy_TB[1] VSS VSS VSS VSS nfet_05v0 L=1.00u W=1.25u nf=1 ad='int((nf+1)/2) * W/nf * 0.18u' as='int((nf+2)/2) * W/nf * 0.18u'
+ pd='2*int((nf+1)/2) * (W/nf + 0.18u)' ps='2*int((nf+2)/2) * (W/nf + 0.18u)' nrd='0.18u / W' nrs='0.18u / W'
+ sa=0 sb=0 sd=0 m=1
XMnota_dummy_TB[0] VSS VSS VSS VSS nfet_05v0 L=1.00u W=1.25u nf=1 ad='int((nf+1)/2) * W/nf * 0.18u' as='int((nf+2)/2) * W/nf * 0.18u'
+ pd='2*int((nf+1)/2) * (W/nf + 0.18u)' ps='2*int((nf+2)/2) * (W/nf + 0.18u)' nrd='0.18u / W' nrs='0.18u / W'
+ sa=0 sb=0 sd=0 m=1
XMnbias_dummy_L[3] VSS VSS VSS VSS nfet_05v0 L=1.00u W=3.00u nf=1 ad='int((nf+1)/2) * W/nf * 0.18u' as='int((nf+2)/2) * W/nf * 0.18u'
+ pd='2*int((nf+1)/2) * (W/nf + 0.18u)' ps='2*int((nf+2)/2) * (W/nf + 0.18u)' nrd='0.18u / W' nrs='0.18u / W'
+ sa=0 sb=0 sd=0 m=1
XMnbias_dummy_L[2] VSS VSS VSS VSS nfet_05v0 L=1.00u W=3.00u nf=1 ad='int((nf+1)/2) * W/nf * 0.18u' as='int((nf+2)/2) * W/nf * 0.18u'
+ pd='2*int((nf+1)/2) * (W/nf + 0.18u)' ps='2*int((nf+2)/2) * (W/nf + 0.18u)' nrd='0.18u / W' nrs='0.18u / W'
+ sa=0 sb=0 sd=0 m=1
XMnbias_dummy_L[1] VSS VSS VSS VSS nfet_05v0 L=1.00u W=3.00u nf=1 ad='int((nf+1)/2) * W/nf * 0.18u' as='int((nf+2)/2) * W/nf * 0.18u'
+ pd='2*int((nf+1)/2) * (W/nf + 0.18u)' ps='2*int((nf+2)/2) * (W/nf + 0.18u)' nrd='0.18u / W' nrs='0.18u / W'
+ sa=0 sb=0 sd=0 m=1
XMnbias_dummy_L[0] VSS VSS VSS VSS nfet_05v0 L=1.00u W=3.00u nf=1 ad='int((nf+1)/2) * W/nf * 0.18u' as='int((nf+2)/2) * W/nf * 0.18u'
+ pd='2*int((nf+1)/2) * (W/nf + 0.18u)' ps='2*int((nf+2)/2) * (W/nf + 0.18u)' nrd='0.18u / W' nrs='0.18u / W'
+ sa=0 sb=0 sd=0 m=1
XMnbias_dummy_TB[7] VSS VSS VSS VSS nfet_05v0 L=1.00u W=3.00u nf=1 ad='int((nf+1)/2) * W/nf * 0.18u'
+ as='int((nf+2)/2) * W/nf * 0.18u' pd='2*int((nf+1)/2) * (W/nf + 0.18u)' ps='2*int((nf+2)/2) * (W/nf + 0.18u)'
+ nrd='0.18u / W' nrs='0.18u / W' sa=0 sb=0 sd=0 m=1
XMnbias_dummy_TB[6] VSS VSS VSS VSS nfet_05v0 L=1.00u W=3.00u nf=1 ad='int((nf+1)/2) * W/nf * 0.18u'
+ as='int((nf+2)/2) * W/nf * 0.18u' pd='2*int((nf+1)/2) * (W/nf + 0.18u)' ps='2*int((nf+2)/2) * (W/nf + 0.18u)'
+ nrd='0.18u / W' nrs='0.18u / W' sa=0 sb=0 sd=0 m=1
XMnbias_dummy_TB[5] VSS VSS VSS VSS nfet_05v0 L=1.00u W=3.00u nf=1 ad='int((nf+1)/2) * W/nf * 0.18u'
+ as='int((nf+2)/2) * W/nf * 0.18u' pd='2*int((nf+1)/2) * (W/nf + 0.18u)' ps='2*int((nf+2)/2) * (W/nf + 0.18u)'
+ nrd='0.18u / W' nrs='0.18u / W' sa=0 sb=0 sd=0 m=1
XMnbias_dummy_TB[4] VSS VSS VSS VSS nfet_05v0 L=1.00u W=3.00u nf=1 ad='int((nf+1)/2) * W/nf * 0.18u'
+ as='int((nf+2)/2) * W/nf * 0.18u' pd='2*int((nf+1)/2) * (W/nf + 0.18u)' ps='2*int((nf+2)/2) * (W/nf + 0.18u)'
+ nrd='0.18u / W' nrs='0.18u / W' sa=0 sb=0 sd=0 m=1
XMnbias_dummy_TB[3] VSS VSS VSS VSS nfet_05v0 L=1.00u W=3.00u nf=1 ad='int((nf+1)/2) * W/nf * 0.18u'
+ as='int((nf+2)/2) * W/nf * 0.18u' pd='2*int((nf+1)/2) * (W/nf + 0.18u)' ps='2*int((nf+2)/2) * (W/nf + 0.18u)'
+ nrd='0.18u / W' nrs='0.18u / W' sa=0 sb=0 sd=0 m=1
XMnbias_dummy_TB[2] VSS VSS VSS VSS nfet_05v0 L=1.00u W=3.00u nf=1 ad='int((nf+1)/2) * W/nf * 0.18u'
+ as='int((nf+2)/2) * W/nf * 0.18u' pd='2*int((nf+1)/2) * (W/nf + 0.18u)' ps='2*int((nf+2)/2) * (W/nf + 0.18u)'
+ nrd='0.18u / W' nrs='0.18u / W' sa=0 sb=0 sd=0 m=1
XMnbias_dummy_TB[1] VSS VSS VSS VSS nfet_05v0 L=1.00u W=3.00u nf=1 ad='int((nf+1)/2) * W/nf * 0.18u'
+ as='int((nf+2)/2) * W/nf * 0.18u' pd='2*int((nf+1)/2) * (W/nf + 0.18u)' ps='2*int((nf+2)/2) * (W/nf + 0.18u)'
+ nrd='0.18u / W' nrs='0.18u / W' sa=0 sb=0 sd=0 m=1
XMnbias_dummy_TB[0] VSS VSS VSS VSS nfet_05v0 L=1.00u W=3.00u nf=1 ad='int((nf+1)/2) * W/nf * 0.18u'
+ as='int((nf+2)/2) * W/nf * 0.18u' pd='2*int((nf+1)/2) * (W/nf + 0.18u)' ps='2*int((nf+2)/2) * (W/nf + 0.18u)'
+ nrd='0.18u / W' nrs='0.18u / W' sa=0 sb=0 sd=0 m=1
XMpenota1 Vbp2 ENp VDD VDD pfet_05v0 L=0.5u W=2u nf=1 ad='int((nf+1)/2) * W/nf * 0.18u' as='int((nf+2)/2) * W/nf * 0.18u'
+ pd='2*int((nf+1)/2) * (W/nf + 0.18u)' ps='2*int((nf+2)/2) * (W/nf + 0.18u)' nrd='0.18u / W' nrs='0.18u / W'
+ sa=0 sb=0 sd=0 m=1
XMpenota2 Vbp1 ENp VDD VDD pfet_05v0 L=0.5u W=2u nf=1 ad='int((nf+1)/2) * W/nf * 0.18u' as='int((nf+2)/2) * W/nf * 0.18u'
+ pd='2*int((nf+1)/2) * (W/nf + 0.18u)' ps='2*int((nf+2)/2) * (W/nf + 0.18u)' nrd='0.18u / W' nrs='0.18u / W'
+ sa=0 sb=0 sd=0 m=1
XMnenota1 Vbn2 ENn VSS VSS nfet_05v0 L=0.6u W=2u nf=1 ad='int((nf+1)/2) * W/nf * 0.18u' as='int((nf+2)/2) * W/nf * 0.18u'
+ pd='2*int((nf+1)/2) * (W/nf + 0.18u)' ps='2*int((nf+2)/2) * (W/nf + 0.18u)' nrd='0.18u / W' nrs='0.18u / W'
+ sa=0 sb=0 sd=0 m=1
XMnenota2 Vbn1 ENn VSS VSS nfet_05v0 L=0.6u W=2u nf=1 ad='int((nf+1)/2) * W/nf * 0.18u' as='int((nf+2)/2) * W/nf * 0.18u'
+ pd='2*int((nf+1)/2) * (W/nf + 0.18u)' ps='2*int((nf+2)/2) * (W/nf + 0.18u)' nrd='0.18u / W' nrs='0.18u / W'
+ sa=0 sb=0 sd=0 m=1
XMnenota3 IBIAS ENp Vbn1 VSS nfet_05v0 L=0.6u W=2u nf=1 ad='int((nf+1)/2) * W/nf * 0.18u' as='int((nf+2)/2) * W/nf * 0.18u'
+ pd='2*int((nf+1)/2) * (W/nf + 0.18u)' ps='2*int((nf+2)/2) * (W/nf + 0.18u)' nrd='0.18u / W' nrs='0.18u / W'
+ sa=0 sb=0 sd=0 m=1
.ends

.end
